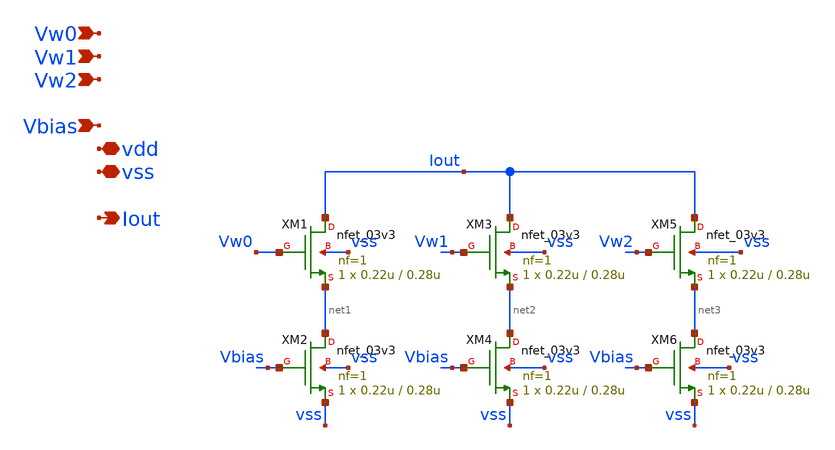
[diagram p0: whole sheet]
** sch_path: analog/dac/3bit_NMOS_DAC.sch
**.subckt 3bit_NMOS_DAC Vw0 vdd vss Iout Vw1 Vw2 Vbias
*.ipin Vw0
*.iopin vdd
*.iopin vss
*.opin Iout
*.ipin Vw1
*.ipin Vw2
*.ipin Vbias
XM1 Iout Vw0 net1 vss nfet_03v3 L=0.28u W=0.22u nf=1 ad='int((nf+1)/2) * W/nf * 0.18u' as='int((nf+2)/2) * W/nf * 0.18u'
+ pd='2*int((nf+1)/2) * (W/nf + 0.18u)' ps='2*int((nf+2)/2) * (W/nf + 0.18u)' nrd='0.18u / W' nrs='0.18u / W'
+ sa=0 sb=0 sd=0 m=1
XM2 net1 Vbias vss vss nfet_03v3 L=0.28u W=0.22u nf=1 ad='int((nf+1)/2) * W/nf * 0.18u' as='int((nf+2)/2) * W/nf * 0.18u'
+ pd='2*int((nf+1)/2) * (W/nf + 0.18u)' ps='2*int((nf+2)/2) * (W/nf + 0.18u)' nrd='0.18u / W' nrs='0.18u / W'
+ sa=0 sb=0 sd=0 m=1
XM3 Iout Vw1 net2 vss nfet_03v3 L=0.28u W=0.22u nf=1 ad='int((nf+1)/2) * W/nf * 0.18u' as='int((nf+2)/2) * W/nf * 0.18u'
+ pd='2*int((nf+1)/2) * (W/nf + 0.18u)' ps='2*int((nf+2)/2) * (W/nf + 0.18u)' nrd='0.18u / W' nrs='0.18u / W'
+ sa=0 sb=0 sd=0 m=1
XM4 net2 Vbias vss vss nfet_03v3 L=0.28u W=0.22u nf=1 ad='int((nf+1)/2) * W/nf * 0.18u' as='int((nf+2)/2) * W/nf * 0.18u'
+ pd='2*int((nf+1)/2) * (W/nf + 0.18u)' ps='2*int((nf+2)/2) * (W/nf + 0.18u)' nrd='0.18u / W' nrs='0.18u / W'
+ sa=0 sb=0 sd=0 m=1
XM5 Iout Vw2 net3 vss nfet_03v3 L=0.28u W=0.22u nf=1 ad='int((nf+1)/2) * W/nf * 0.18u' as='int((nf+2)/2) * W/nf * 0.18u'
+ pd='2*int((nf+1)/2) * (W/nf + 0.18u)' ps='2*int((nf+2)/2) * (W/nf + 0.18u)' nrd='0.18u / W' nrs='0.18u / W'
+ sa=0 sb=0 sd=0 m=1
XM6 net3 Vbias vss vss nfet_03v3 L=0.28u W=0.22u nf=1 ad='int((nf+1)/2) * W/nf * 0.18u' as='int((nf+2)/2) * W/nf * 0.18u'
+ pd='2*int((nf+1)/2) * (W/nf + 0.18u)' ps='2*int((nf+2)/2) * (W/nf + 0.18u)' nrd='0.18u / W' nrs='0.18u / W'
+ sa=0 sb=0 sd=0 m=1
**.ends
.end
